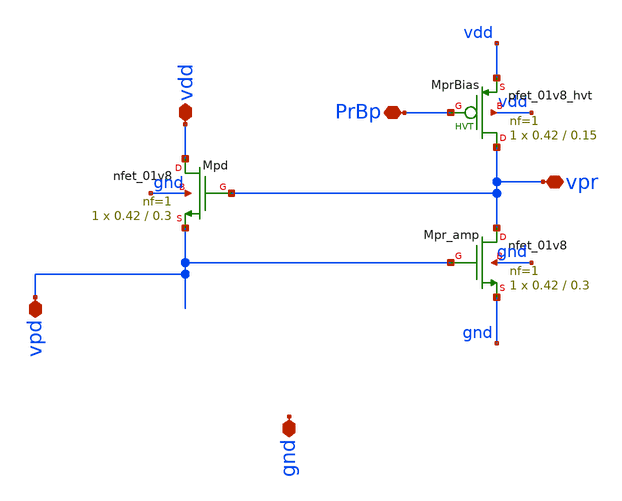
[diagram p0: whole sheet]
** sch_path: analog/xschem/PixelPhotoreceptor.sch
**.subckt PixelPhotoreceptor PrBp vdd vpd gnd vpr
*.iopin PrBp
*.iopin vdd
*.iopin vpd
*.iopin gnd
*.iopin vpr
XMpd vdd vpr vpd gnd sky130_fd_pr__nfet_01v8 L=0.3 W=0.42 nf=1 ad='int((1 + 1)/2) * 0.42 / 1 * 0.29'
+ as='int((1 + 2)/2) * 0.42 / 1 * 0.29' pd='2*int((1 + 1)/2) * (0.42 / 1 + 0.29)' ps='2*int((1 + 2)/2) * (0.42 / 1 + 0.29)'
+ nrd='0.29 / 0.42 ' nrs='0.29 / 0.42 ' sa=0 sb=0 sd=0 mult=1 m=1
XMpr_amp vpr vpd gnd gnd sky130_fd_pr__nfet_01v8 L=0.3 W=0.42 nf=1 ad='int((1 + 1)/2) * 0.42 / 1 * 0.29'
+ as='int((1 + 2)/2) * 0.42 / 1 * 0.29' pd='2*int((1 + 1)/2) * (0.42 / 1 + 0.29)' ps='2*int((1 + 2)/2) * (0.42 / 1 + 0.29)'
+ nrd='0.29 / 0.42 ' nrs='0.29 / 0.42 ' sa=0 sb=0 sd=0 mult=1 m=1
XMprBias vpr PrBp vdd vdd sky130_fd_pr__pfet_01v8_hvt L=0.15 W=0.42 nf=1 ad='int((1 + 1)/2) * 0.42 / 1 * 0.29'
+ as='int((1 + 2)/2) * 0.42 / 1 * 0.29' pd='2*int((1 + 1)/2) * (0.42 / 1 + 0.29)' ps='2*int((1 + 2)/2) * (0.42 / 1 + 0.29)'
+ nrd='0.29 / 0.42 ' nrs='0.29 / 0.42 ' sa=0 sb=0 sd=0 mult=1 m=1
**.ends
.end
